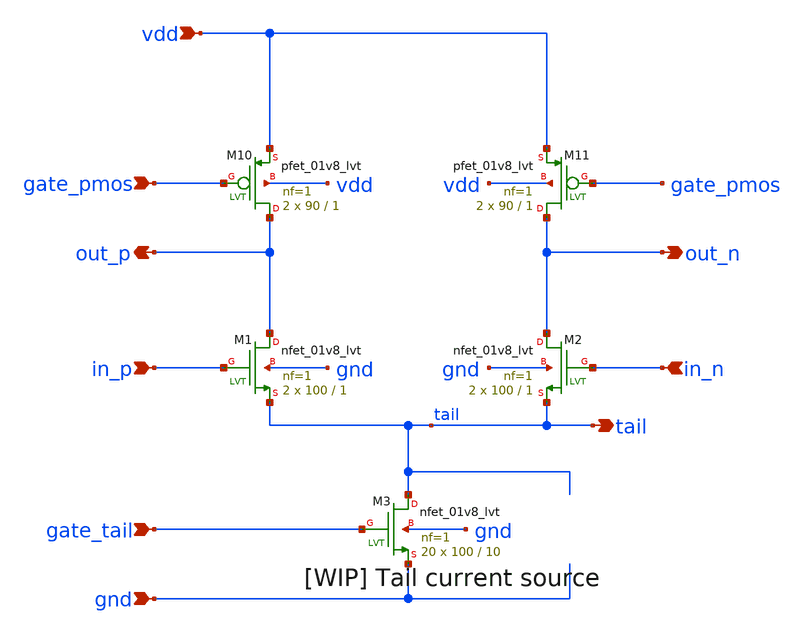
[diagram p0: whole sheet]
** sch_path: Amplifiers/OTA/OTA.sch
**.subckt OTA gate_pmos vdd in_p in_n gnd out_p out_n gate_tail tail
*.ipin gate_pmos
*.ipin vdd
*.ipin in_p
*.ipin in_n
*.ipin gnd
*.opin out_p
*.opin out_n
*.ipin gate_tail
*.opin tail
XM1 out_p in_p tail gnd sky130_fd_pr__nfet_01v8_lvt L=1 W=100 nf=1 ad='int((nf+1)/2) * W/nf * 0.29' as='int((nf+2)/2) * W/nf * 0.29'
+ pd='2*int((nf+1)/2) * (W/nf + 0.29)' ps='2*int((nf+2)/2) * (W/nf + 0.29)' nrd='0.29 / W' nrs='0.29 / W'
+ sa=0 sb=0 sd=0 mult=2 m=2
XM2 out_n in_n tail gnd sky130_fd_pr__nfet_01v8_lvt L=1 W=100 nf=1 ad='int((nf+1)/2) * W/nf * 0.29' as='int((nf+2)/2) * W/nf * 0.29'
+ pd='2*int((nf+1)/2) * (W/nf + 0.29)' ps='2*int((nf+2)/2) * (W/nf + 0.29)' nrd='0.29 / W' nrs='0.29 / W'
+ sa=0 sb=0 sd=0 mult=2 m=2
XM10 out_p gate_pmos vdd vdd sky130_fd_pr__pfet_01v8_lvt L=1 W=90 nf=1 ad='int((1 + 1)/2) * 90 / 1 * 0.29'
+ as='int((1 + 2)/2) * 90 / 1 * 0.29' pd='2*int((1 + 1)/2) * (90 / 1 + 0.29)' ps='2*int((1 + 2)/2) * (90 / 1 + 0.29)'
+ nrd='0.29 / 90 ' nrs='0.29 / 90 ' sa=0 sb=0 sd=0 mult=2 m=2
XM11 out_n gate_pmos vdd vdd sky130_fd_pr__pfet_01v8_lvt L=1 W=90 nf=1 ad='int((1 + 1)/2) * 90 / 1 * 0.29'
+ as='int((1 + 2)/2) * 90 / 1 * 0.29' pd='2*int((1 + 1)/2) * (90 / 1 + 0.29)' ps='2*int((1 + 2)/2) * (90 / 1 + 0.29)'
+ nrd='0.29 / 90 ' nrs='0.29 / 90 ' sa=0 sb=0 sd=0 mult=2 m=2
XM3 tail gate_tail gnd gnd sky130_fd_pr__nfet_01v8_lvt L=10 W=100 nf=1 ad='int((nf+1)/2) * W/nf * 0.29'
+ as='int((nf+2)/2) * W/nf * 0.29' pd='2*int((nf+1)/2) * (W/nf + 0.29)' ps='2*int((nf+2)/2) * (W/nf + 0.29)'
+ nrd='0.29 / W' nrs='0.29 / W' sa=0 sb=0 sd=0 mult=20 m=20
**.ends
.end
